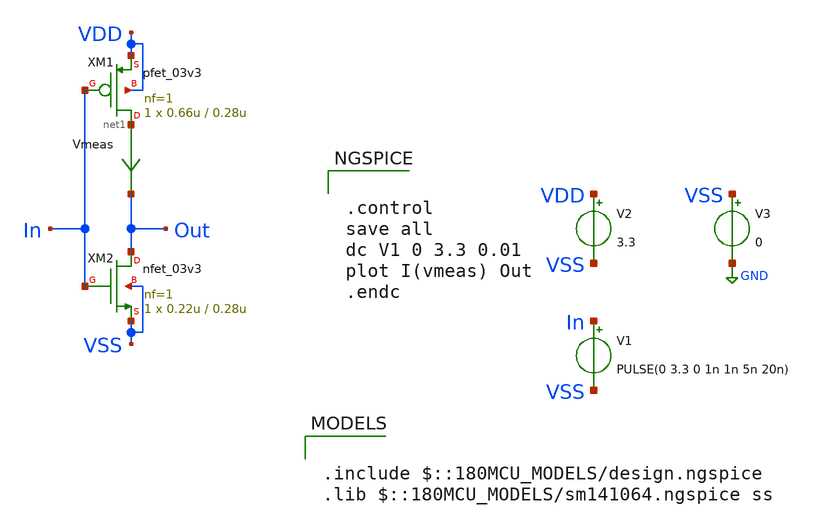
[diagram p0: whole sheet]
** sch_path: week02_current_diffpair/tugas5_cascode_current_mirror/skematik-hitam.sch
**.subckt skematik-hitam
XM1 net1 In VDD VDD pfet_03v3 L=0.28u W=0.66u nf=1 ad='int((nf+1)/2) * W/nf * 0.18u' as='int((nf+2)/2) * W/nf * 0.18u'
+ pd='2*int((nf+1)/2) * (W/nf + 0.18u)' ps='2*int((nf+2)/2) * (W/nf + 0.18u)' nrd='0.18u / W' nrs='0.18u / W'
+ sa=0 sb=0 sd=0 m=1
XM2 Out In VSS VSS nfet_03v3 L=0.28u W=0.22u nf=1 ad='int((nf+1)/2) * W/nf * 0.18u' as='int((nf+2)/2) * W/nf * 0.18u'
+ pd='2*int((nf+1)/2) * (W/nf + 0.18u)' ps='2*int((nf+2)/2) * (W/nf + 0.18u)' nrd='0.18u / W' nrs='0.18u / W'
+ sa=0 sb=0 sd=0 m=1
V1 In VSS PULSE(0 3.3 0 1n 1n 5n 20n)
V2 VDD VSS 3.3
V3 VSS GND 0
Vmeas net1 Out 0
.save i(vmeas)
**** begin user architecture code

.include $::180MCU_MODELS/design.ngspice
.lib $::180MCU_MODELS/sm141064.ngspice ss



.control
save all
dc V1 0 3.3 0.01
plot I(vmeas) Out
.endc


**** end user architecture code
**.ends
.GLOBAL GND
.end
